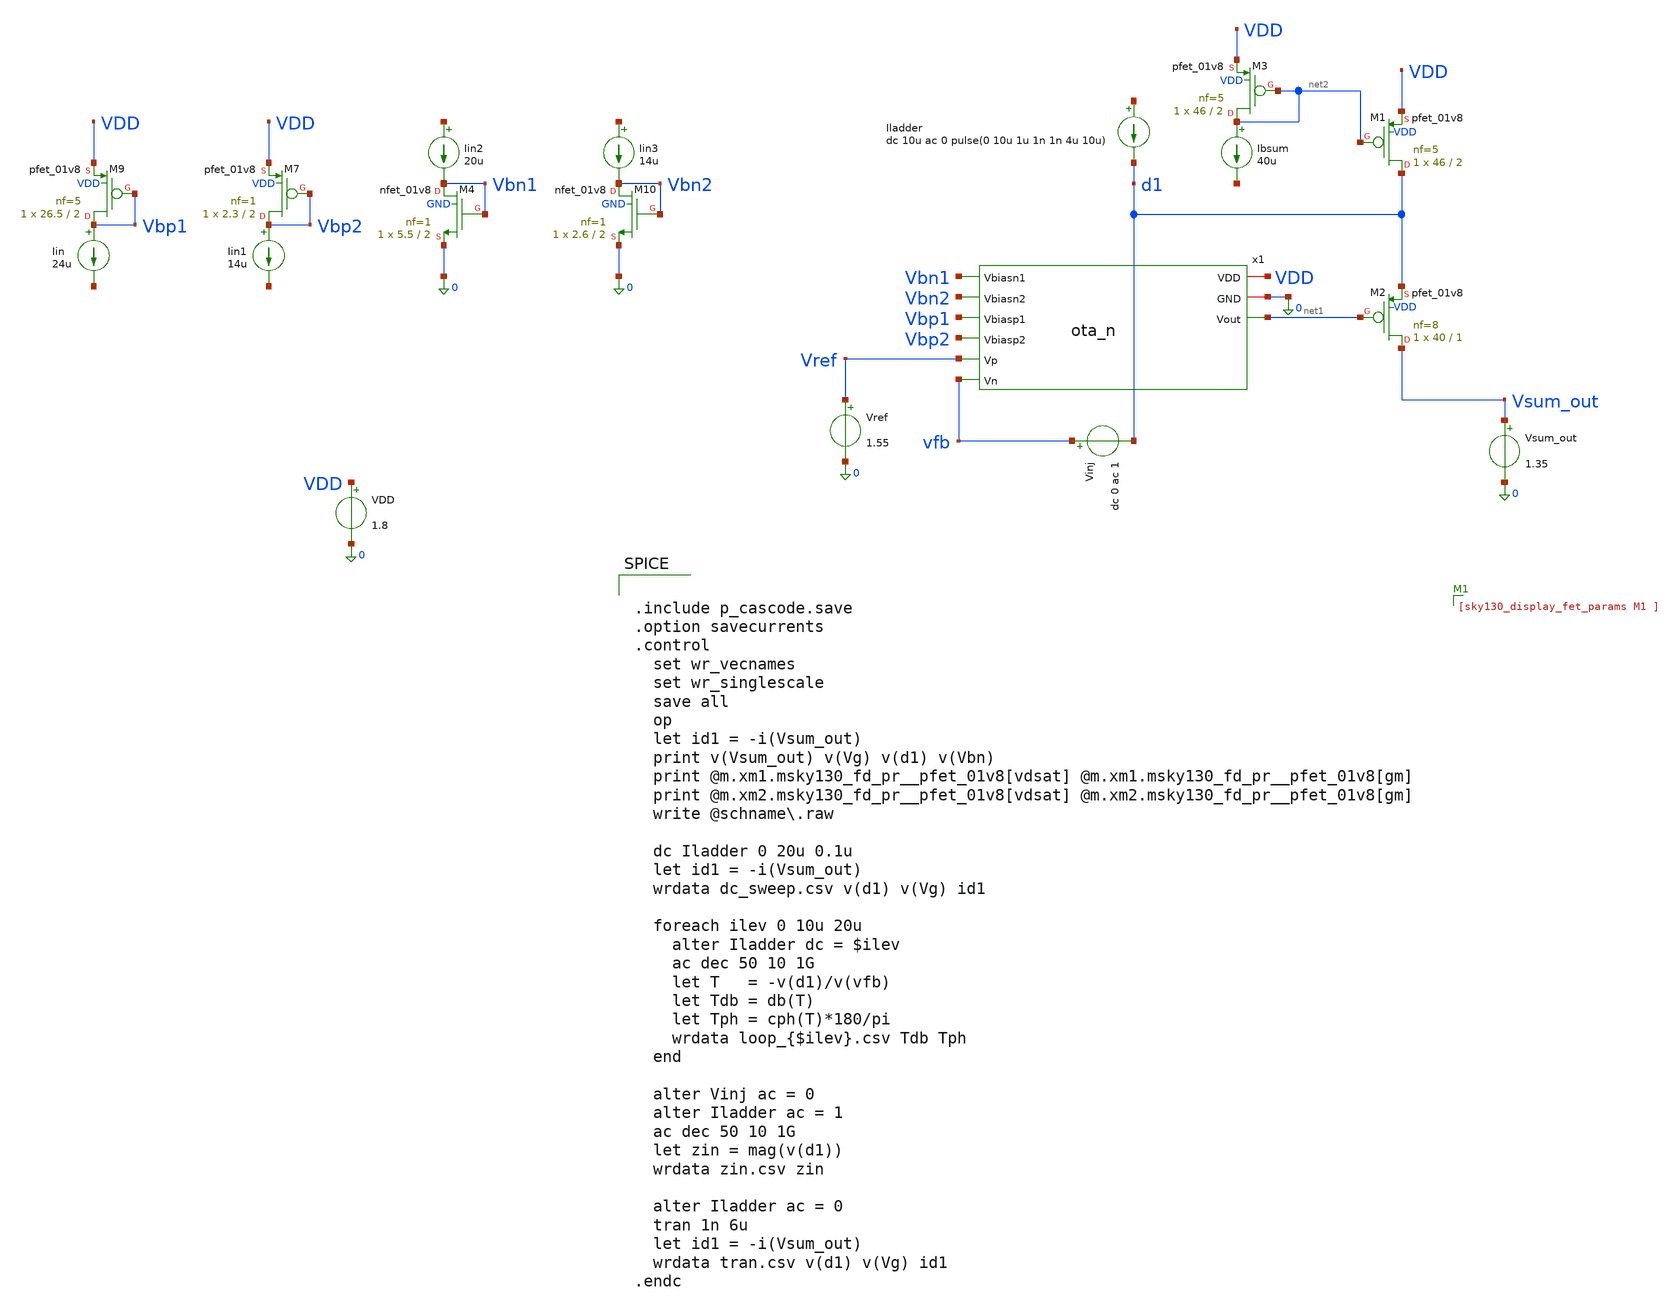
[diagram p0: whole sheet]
** sch_path: sch/cascode/p_cascode.sch
**.subckt p_cascode
Vref Vref 0 1.55
.save i(vref)
VDD VDD 0 1.8
.save i(vdd)
Iladder net3 d1 dc 10u ac 0 pulse(0 10u 1u 1n 1n 4u 10u)
Vsum_out Vsum_out 0 1.35
.save i(vsum_out)
Vinj vfb d1 dc 0 ac 1
.save i(vinj)
x1 VDD 0 Vbn1 Vbn2 Vbp1 Vbp2 Vref vfb net1 ota_n
XM1 d1 net2 VDD VDD sky130_fd_pr__pfet_01v8 L=2 W=46 nf=5 ad='int((5 + 1)/2) * 46 / 5 * 0.29' as='int((5 + 2)/2) * 46 / 5 * 0.29'
+ pd='2*int((5 + 1)/2) * (46 / 5 + 0.29)' ps='2*int((5 + 2)/2) * (46 / 5 + 0.29)' nrd='0.29 / 46 ' nrs='0.29 / 46 '
+ sa=0 sb=0 sd=0 mult=1 m=1
XM2 Vsum_out net1 d1 VDD sky130_fd_pr__pfet_01v8 L=1 W=40 nf=8 ad='int((8 + 1)/2) * 40 / 8 * 0.29' as='int((8 + 2)/2) * 40 / 8 * 0.29'
+ pd='2*int((8 + 1)/2) * (40 / 8 + 0.29)' ps='2*int((8 + 2)/2) * (40 / 8 + 0.29)' nrd='0.29 / 40 ' nrs='0.29 / 40 '
+ sa=0 sb=0 sd=0 mult=1 m=1
XM3 net2 net2 VDD VDD sky130_fd_pr__pfet_01v8 L=2 W=46 nf=5 ad='int((5 + 1)/2) * 46 / 5 * 0.29' as='int((5 + 2)/2) * 46 / 5 * 0.29'
+ pd='2*int((5 + 1)/2) * (46 / 5 + 0.29)' ps='2*int((5 + 2)/2) * (46 / 5 + 0.29)' nrd='0.29 / 46 ' nrs='0.29 / 46 '
+ sa=0 sb=0 sd=0 mult=1 m=1
Ibsum net2 net4 40u
Iin Vbp1 net5 24u
Iin1 Vbp2 net6 14u
Iin2 net7 Vbn1 20u
Iin3 net8 Vbn2 14u
XM9 Vbp1 Vbp1 VDD VDD sky130_fd_pr__pfet_01v8 L=2 W=26.5 nf=5 ad='int((5 + 1)/2) * 26.5 / 5 * 0.29' as='int((5 + 2)/2) * 26.5 / 5 * 0.29'
+ pd='2*int((5 + 1)/2) * (26.5 / 5 + 0.29)' ps='2*int((5 + 2)/2) * (26.5 / 5 + 0.29)' nrd='0.29 / 26.5 '
+ nrs='0.29 / 26.5 ' sa=0 sb=0 sd=0 mult=1 m=1
XM7 Vbp2 Vbp2 VDD VDD sky130_fd_pr__pfet_01v8 L=2 W=2.3 nf=1 ad='int((1 + 1)/2) * 2.3 / 1 * 0.29' as='int((1 + 2)/2) * 2.3 / 1 * 0.29'
+ pd='2*int((1 + 1)/2) * (2.3 / 1 + 0.29)' ps='2*int((1 + 2)/2) * (2.3 / 1 + 0.29)' nrd='0.29 / 2.3 ' nrs='0.29 / 2.3 '
+ sa=0 sb=0 sd=0 mult=1 m=1
XM10 Vbn2 Vbn2 0 GND sky130_fd_pr__nfet_01v8 L=2 W=2.6 nf=1 ad='int((1 + 1)/2) * 2.6 / 1 * 0.29' as='int((1 + 2)/2) * 2.6 / 1 * 0.29'
+ pd='2*int((1 + 1)/2) * (2.6 / 1 + 0.29)' ps='2*int((1 + 2)/2) * (2.6 / 1 + 0.29)' nrd='0.29 / 2.6 ' nrs='0.29 / 2.6 '
+ sa=0 sb=0 sd=0 mult=1 m=1
XM4 Vbn1 Vbn1 0 GND sky130_fd_pr__nfet_01v8 L=2 W=5.5 nf=1 ad='int((1 + 1)/2) * 5.5 / 1 * 0.29' as='int((1 + 2)/2) * 5.5 / 1 * 0.29'
+ pd='2*int((1 + 1)/2) * (5.5 / 1 + 0.29)' ps='2*int((1 + 2)/2) * (5.5 / 1 + 0.29)' nrd='0.29 / 5.5 ' nrs='0.29 / 5.5 '
+ sa=0 sb=0 sd=0 mult=1 m=1
**** begin user architecture code

** opencircuitdesign pdks install
.lib $::SKYWATER_MODELS/sky130.lib.spice tt
.include $::SKYWATER_STDCELLS/sky130_fd_sc_hd.spice



.include p_cascode.save
.option savecurrents
.control
  set wr_vecnames
  set wr_singlescale
  save all
  op
  let id1 = -i(Vsum_out)
  print v(Vsum_out) v(Vg) v(d1) v(Vbn)
  print @m.xm1.msky130_fd_pr__pfet_01v8[vdsat] @m.xm1.msky130_fd_pr__pfet_01v8[gm]
  print @m.xm2.msky130_fd_pr__pfet_01v8[vdsat] @m.xm2.msky130_fd_pr__pfet_01v8[gm]
  write @schname\.raw

  dc Iladder 0 20u 0.1u
  let id1 = -i(Vsum_out)
  wrdata dc_sweep.csv v(d1) v(Vg) id1

  foreach ilev 0 10u 20u
    alter Iladder dc = $ilev
    ac dec 50 10 1G
    let T   = -v(d1)/v(vfb)
    let Tdb = db(T)
    let Tph = cph(T)*180/pi
    wrdata loop_{$ilev}.csv Tdb Tph
  end

  alter Vinj ac = 0
  alter Iladder ac = 1
  ac dec 50 10 1G
  let zin = mag(v(d1))
  wrdata zin.csv zin

  alter Iladder ac = 0
  tran 1n 6u
  let id1 = -i(Vsum_out)
  wrdata tran.csv v(d1) v(Vg) id1
.endc


**** end user architecture code
**.ends

* expanding   symbol:  /foss/designs/sar_adc/sch/cascode/ota_n.sym # of pins=9
** sym_path: sch/cascode/ota_n.sym
** sch_path: sch/cascode/ota_n.sch
.subckt ota_n VDD GND Vbiasn1 Vbiasn2 Vbiasp1 Vbiasp2 Vp Vn Vout
*.ipin Vbiasn2
*.opin Vout
*.iopin VDD
*.iopin GND
*.ipin Vp
*.ipin Vn
*.ipin Vbiasp1
*.ipin Vbiasp2
*.ipin Vbiasn1
XM3 net1 Vp Vx GND sky130_fd_pr__nfet_01v8 L=2 W=7.5 nf=1 ad='int((1 + 1)/2) * 7.5 / 1 * 0.29' as='int((1 + 2)/2) * 7.5 / 1 * 0.29'
+ pd='2*int((1 + 1)/2) * (7.5 / 1 + 0.29)' ps='2*int((1 + 2)/2) * (7.5 / 1 + 0.29)' nrd='0.29 / 7.5 ' nrs='0.29 / 7.5 '
+ sa=0 sb=0 sd=0 mult=1 m=1
XM2 Vfold Vn Vx GND sky130_fd_pr__nfet_01v8 L=2 W=7.5 nf=1 ad='int((1 + 1)/2) * 7.5 / 1 * 0.29' as='int((1 + 2)/2) * 7.5 / 1 * 0.29'
+ pd='2*int((1 + 1)/2) * (7.5 / 1 + 0.29)' ps='2*int((1 + 2)/2) * (7.5 / 1 + 0.29)' nrd='0.29 / 7.5 ' nrs='0.29 / 7.5 '
+ sa=0 sb=0 sd=0 mult=1 m=1
XM4 net3 net2 GND GND sky130_fd_pr__nfet_01v8 L=2 W=14 nf=2 ad='int((2 + 1)/2) * 14 / 2 * 0.29' as='int((2 + 2)/2) * 14 / 2 * 0.29'
+ pd='2*int((2 + 1)/2) * (14 / 2 + 0.29)' ps='2*int((2 + 2)/2) * (14 / 2 + 0.29)' nrd='0.29 / 14 ' nrs='0.29 / 14 '
+ sa=0 sb=0 sd=0 mult=1 m=1
XM5 net4 net2 GND GND sky130_fd_pr__nfet_01v8 L=2 W=14 nf=2 ad='int((2 + 1)/2) * 14 / 2 * 0.29' as='int((2 + 2)/2) * 14 / 2 * 0.29'
+ pd='2*int((2 + 1)/2) * (14 / 2 + 0.29)' ps='2*int((2 + 2)/2) * (14 / 2 + 0.29)' nrd='0.29 / 14 ' nrs='0.29 / 14 '
+ sa=0 sb=0 sd=0 mult=1 m=1
XM8 net1 Vbiasp1 VDD VDD sky130_fd_pr__pfet_01v8 L=2 W=26.5 nf=5 ad='int((5 + 1)/2) * 26.5 / 5 * 0.29'
+ as='int((5 + 2)/2) * 26.5 / 5 * 0.29' pd='2*int((5 + 1)/2) * (26.5 / 5 + 0.29)' ps='2*int((5 + 2)/2) * (26.5 / 5 + 0.29)'
+ nrd='0.29 / 26.5 ' nrs='0.29 / 26.5 ' sa=0 sb=0 sd=0 mult=1 m=1
XM9 Vfold Vbiasp1 VDD VDD sky130_fd_pr__pfet_01v8 L=2 W=26.5 nf=5 ad='int((5 + 1)/2) * 26.5 / 5 * 0.29'
+ as='int((5 + 2)/2) * 26.5 / 5 * 0.29' pd='2*int((5 + 1)/2) * (26.5 / 5 + 0.29)' ps='2*int((5 + 2)/2) * (26.5 / 5 + 0.29)'
+ nrd='0.29 / 26.5 ' nrs='0.29 / 26.5 ' sa=0 sb=0 sd=0 mult=1 m=1
XM1 Vx Vbiasn1 GND GND sky130_fd_pr__nfet_01v8 L=2 W=5.5 nf=1 ad='int((1 + 1)/2) * 5.5 / 1 * 0.29' as='int((1 + 2)/2) * 5.5 / 1 * 0.29'
+ pd='2*int((1 + 1)/2) * (5.5 / 1 + 0.29)' ps='2*int((1 + 2)/2) * (5.5 / 1 + 0.29)' nrd='0.29 / 5.5 ' nrs='0.29 / 5.5 '
+ sa=0 sb=0 sd=0 mult=1 m=1
XM6 net2 Vbiasp2 net1 VDD sky130_fd_pr__pfet_01v8 L=2 W=13 nf=2 ad='int((2 + 1)/2) * 13 / 2 * 0.29' as='int((2 + 2)/2) * 13 / 2 * 0.29'
+ pd='2*int((2 + 1)/2) * (13 / 2 + 0.29)' ps='2*int((2 + 2)/2) * (13 / 2 + 0.29)' nrd='0.29 / 13 ' nrs='0.29 / 13 '
+ sa=0 sb=0 sd=0 mult=1 m=1
XM7 Vout Vbiasp2 Vfold VDD sky130_fd_pr__pfet_01v8 L=2 W=13 nf=2 ad='int((2 + 1)/2) * 13 / 2 * 0.29'
+ as='int((2 + 2)/2) * 13 / 2 * 0.29' pd='2*int((2 + 1)/2) * (13 / 2 + 0.29)' ps='2*int((2 + 2)/2) * (13 / 2 + 0.29)'
+ nrd='0.29 / 13 ' nrs='0.29 / 13 ' sa=0 sb=0 sd=0 mult=1 m=1
XM10 Vout Vbiasn2 net4 GND sky130_fd_pr__nfet_01v8 L=2 W=26.5 nf=5 ad='int((5 + 1)/2) * 26.5 / 5 * 0.29'
+ as='int((5 + 2)/2) * 26.5 / 5 * 0.29' pd='2*int((5 + 1)/2) * (26.5 / 5 + 0.29)' ps='2*int((5 + 2)/2) * (26.5 / 5 + 0.29)'
+ nrd='0.29 / 26.5 ' nrs='0.29 / 26.5 ' sa=0 sb=0 sd=0 mult=1 m=1
XM11 net2 Vbiasn2 net3 GND sky130_fd_pr__nfet_01v8 L=2 W=26.5 nf=5 ad='int((5 + 1)/2) * 26.5 / 5 * 0.29'
+ as='int((5 + 2)/2) * 26.5 / 5 * 0.29' pd='2*int((5 + 1)/2) * (26.5 / 5 + 0.29)' ps='2*int((5 + 2)/2) * (26.5 / 5 + 0.29)'
+ nrd='0.29 / 26.5 ' nrs='0.29 / 26.5 ' sa=0 sb=0 sd=0 mult=1 m=1
.ends

.end
